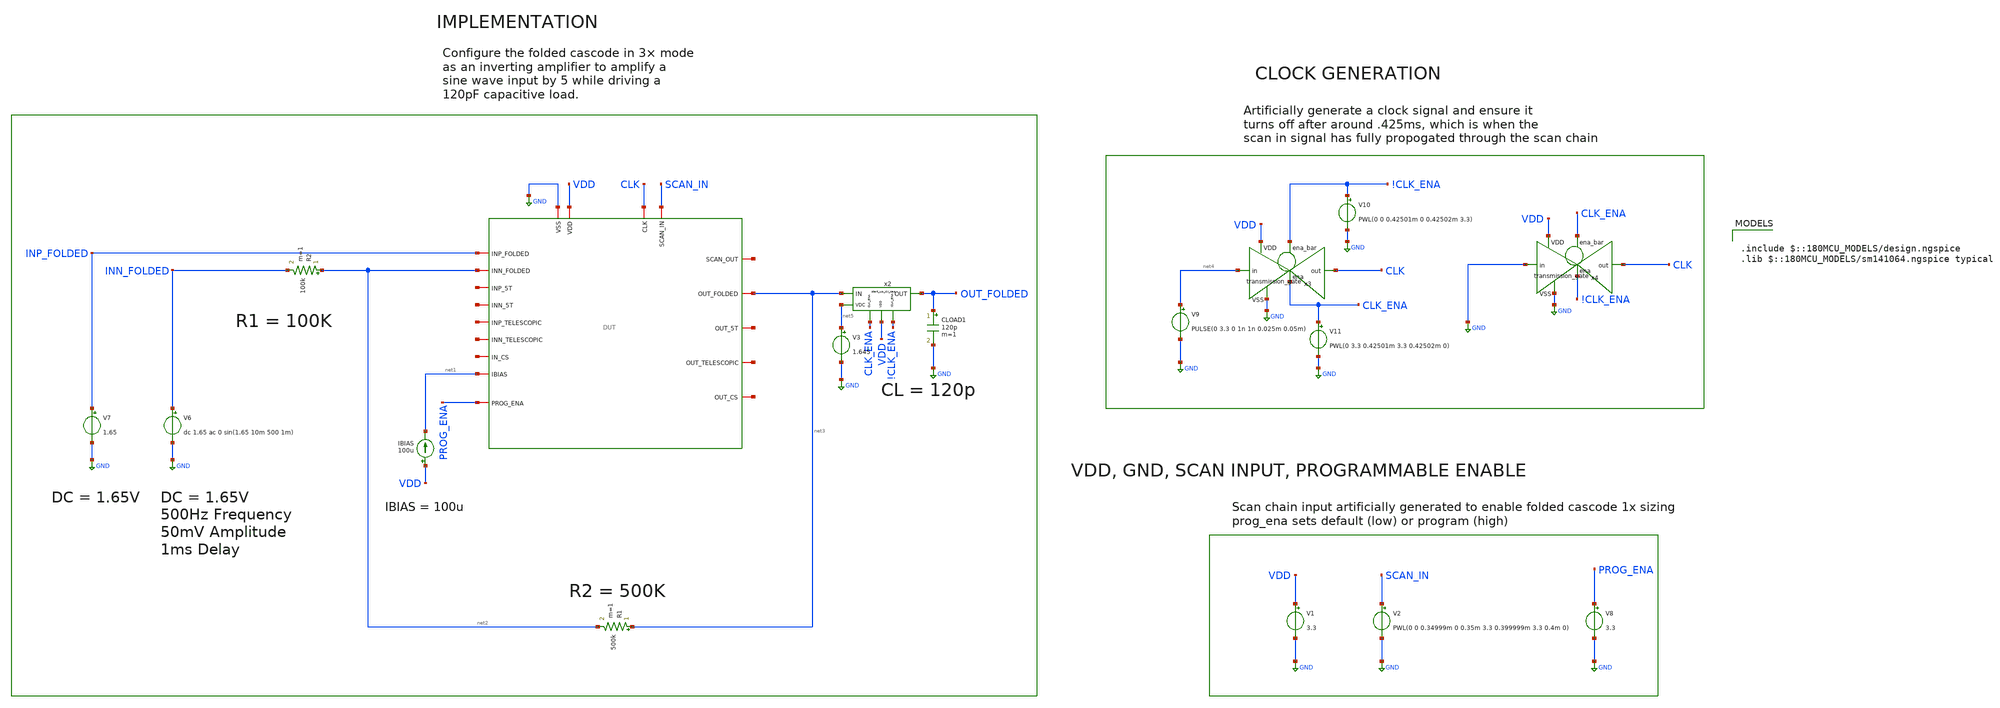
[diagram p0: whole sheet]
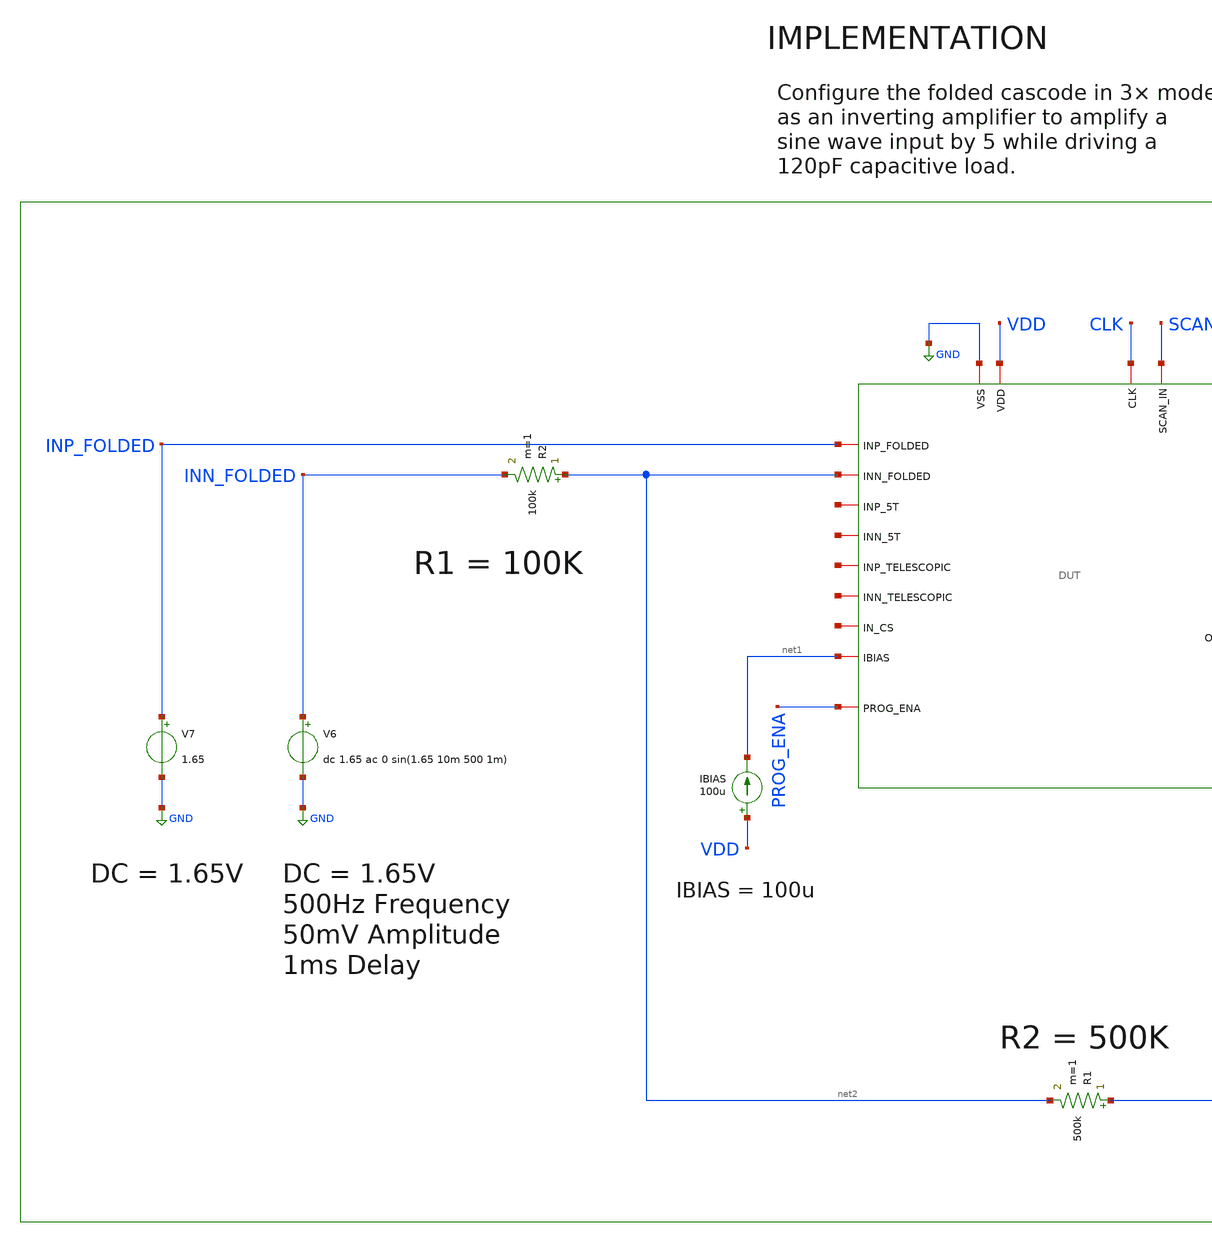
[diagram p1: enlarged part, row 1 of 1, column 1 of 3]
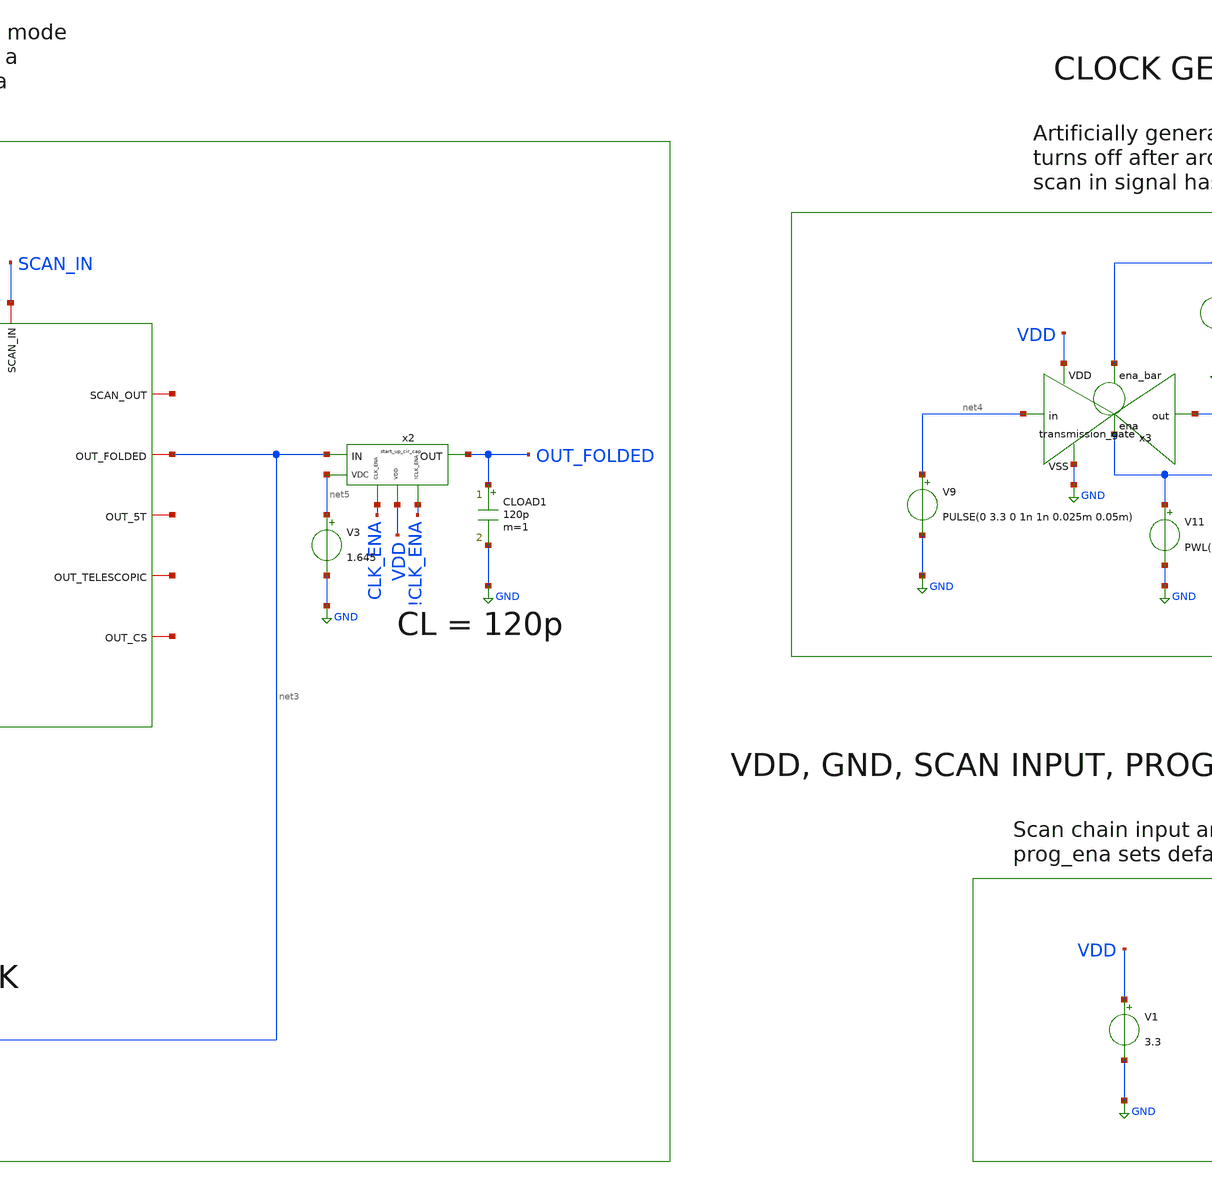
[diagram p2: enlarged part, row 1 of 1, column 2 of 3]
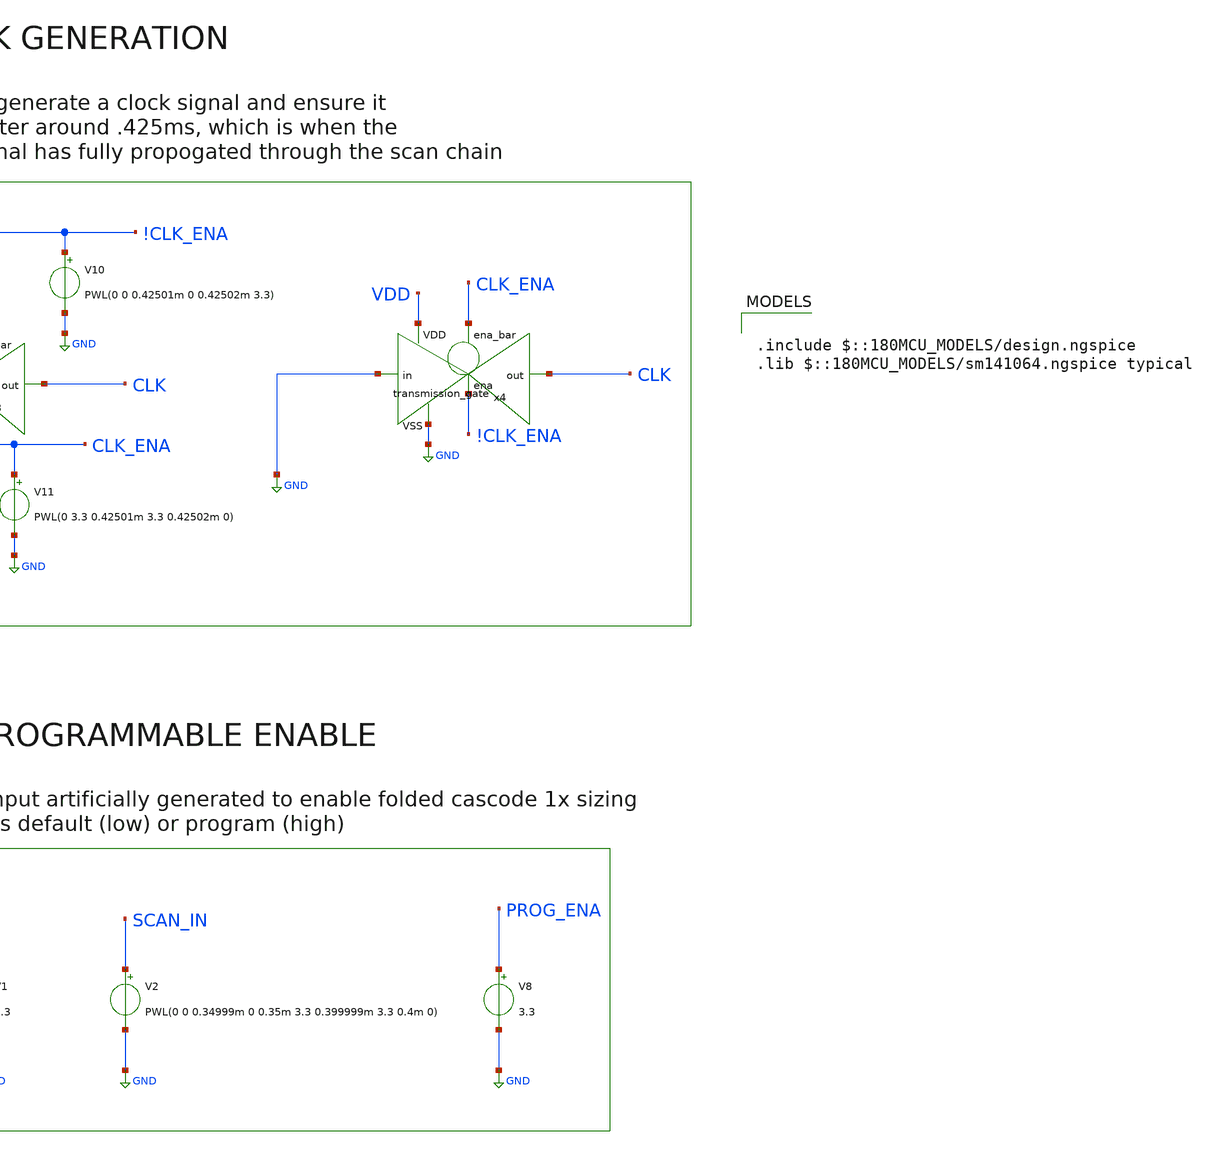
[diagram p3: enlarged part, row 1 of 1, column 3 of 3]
** sch_path: designs/libs/pex/start_up_cir/folded/3x.sch
**.subckt 3x
V1 VDD GND 3.3
IBIAS VDD net1 100u
V7 INP_FOLDED GND 1.65
R2 net2 INN_FOLDED 100k m=1
V6 INN_FOLDED GND dc 1.65 ac 0 sin(1.65 10m 500 1m)
R1 net3 net2 500k m=1
V8 PROG_ENA GND 3.3
V9 net4 GND PULSE(0 3.3 0 1n 1n 0.025m 0.05m)
x3 !CLK_ENA VDD CLK net4 GND CLK_ENA transmission_gate
V10 !CLK_ENA GND PWL(0 0 0.42501m 0 0.42502m 3.3)
V11 CLK_ENA GND PWL(0 3.3 0.42501m 3.3 0.42502m 0)
x4 CLK_ENA VDD CLK GND GND !CLK_ENA transmission_gate
V2 SCAN_IN GND PWL(0 0 0.34999m 0 0.35m 3.3 0.399999m 3.3 0.4m 0)
x1 CLK net6 SCAN_IN GND VDD net3 INP_FOLDED net7 net1 net2 net8 net9 net10 net11 net12 net13 net14
+ PROG_ENA DUT
CLOAD1 OUT_FOLDED GND 120p m=1
V3 net5 GND 1.645
x2 CLK_ENA VDD !CLK_ENA net3 OUT_FOLDED net5 start_up_cir_cap
**** begin user architecture code

.include $::180MCU_MODELS/design.ngspice
.lib $::180MCU_MODELS/sm141064.ngspice typical



.include /foss/designs/libs/pex/DUT.spice
.control
tran 1u 5m

plot v(out_folded) v(inn_folded)
wrdata /foss/designs/libs/pex/start_up_cir/folded/3x.csv v(out_folded) v(inn_folded)

meas tran vout_pp pp v(out_folded) from=2m to=5m
meas tran vin_pp pp v(inn_folded) from=2m to=5m
let gain = vout_pp / vin_pp
print gain

meas tran vout_dc avg v(out_folded) from=2m to=5m
meas tran vin_dc avg v(inn_folded) from=2m to=5m
let dc_offset = vout_dc - vin_dc
let input_offset = dc_offset / 6
print vout_dc vin_dc dc_offset input_offset

let ideal_gain = 5
let gain_error_pct = (ideal_gain - gain) / ideal_gain * 100
print gain_error_pct

meas tran idd avg i(v1) from=2m to=5m
let power = abs(idd) * 3.3
print idd power
.endc


**** end user architecture code
**.ends

* expanding   symbol:  libs/core_digital/schem/transmission_gate.sym # of pins=6
** sym_path: designs/libs/core_digital/schem/transmission_gate.sym
** sch_path: designs/libs/core_digital/schem/transmission_gate.sch
.subckt transmission_gate ena_bar VDD out in VSS ena
*.ipin in
*.ipin ena_bar
*.ipin ena
*.ipin VSS
*.ipin VDD
*.opin out
XM1 in ena_bar out VDD pfet_03v3 L=0.28u W=0.22u nf=1 ad='int((nf+1)/2) * W/nf * 0.18u' as='int((nf+2)/2) * W/nf * 0.18u'
+ pd='2*int((nf+1)/2) * (W/nf + 0.18u)' ps='2*int((nf+2)/2) * (W/nf + 0.18u)' nrd='0.18u / W' nrs='0.18u / W'
+ sa=0 sb=0 sd=0 m=1
XM2 in ena out VSS nfet_03v3 L=0.28u W=0.22u nf=1 ad='int((nf+1)/2) * W/nf * 0.18u' as='int((nf+2)/2) * W/nf * 0.18u'
+ pd='2*int((nf+1)/2) * (W/nf + 0.18u)' ps='2*int((nf+2)/2) * (W/nf + 0.18u)' nrd='0.18u / W' nrs='0.18u / W'
+ sa=0 sb=0 sd=0 m=1
.ends


* expanding   symbol:  libs/core_amps/start_up_cir/start_up_cir_cap.sym # of pins=6
** sym_path: designs/libs/core_amps/start_up_cir/start_up_cir_cap.sym
** sch_path: designs/libs/core_amps/start_up_cir/start_up_cir_cap.sch
.subckt start_up_cir_cap CLK_ENA VDD !CLK_ENA IN OUT VDC
*.ipin IN
*.opin OUT
*.ipin VDC
*.ipin VDD
*.ipin CLK_ENA
*.ipin !CLK_ENA
x2 !CLK_ENA VDD OUT VDC GND CLK_ENA transmission_gate
x5 CLK_ENA VDD OUT IN GND !CLK_ENA transmission_gate
C OUT GND 1n m=1
.ends

.GLOBAL GND
.end
